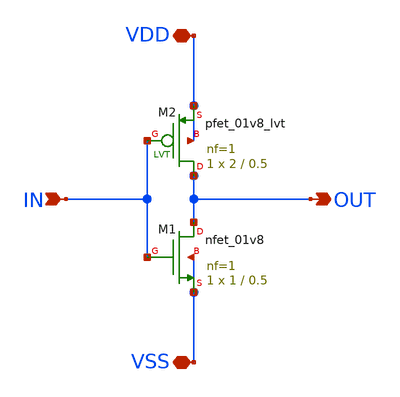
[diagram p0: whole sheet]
** sch_path: schem/inv/inv.sch
**.subckt inv IN VDD VSS OUT
*.ipin IN
*.iopin VDD
*.iopin VSS
*.opin OUT
XM1 OUT IN VSS VSS sky130_fd_pr__nfet_01v8 L=0.5 W=1 nf=1 ad='int((1 + 1)/2) * 1 / 1 * 0.29' as='int((1 + 2)/2) * 1 / 1 * 0.29'
+ pd='2*int((1 + 1)/2) * (1 / 1 + 0.29)' ps='2*int((1 + 2)/2) * (1 / 1 + 0.29)' nrd='0.29 / 1 ' nrs='0.29 / 1 '
+ sa=0 sb=0 sd=0 mult=1 m=1
XM2 OUT IN VDD VDD sky130_fd_pr__pfet_01v8_lvt L=0.5 W=2 nf=1 ad='int((1 + 1)/2) * 2 / 1 * 0.29' as='int((1 + 2)/2) * 2 / 1 * 0.29'
+ pd='2*int((1 + 1)/2) * (2 / 1 + 0.29)' ps='2*int((1 + 2)/2) * (2 / 1 + 0.29)' nrd='0.29 / 2 ' nrs='0.29 / 2 '
+ sa=0 sb=0 sd=0 mult=1 m=1
**.ends
.end
